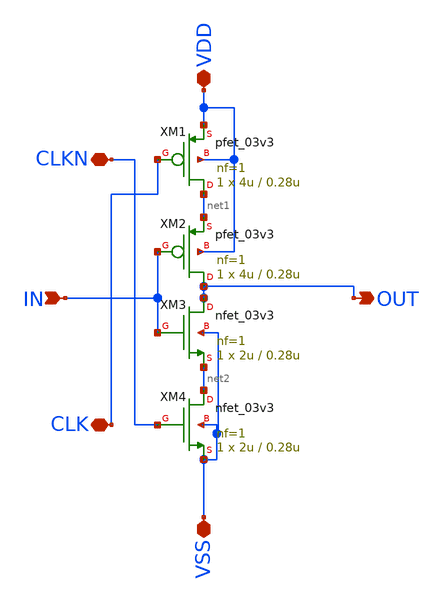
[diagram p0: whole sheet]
** sch_path: CAD6/DFF_Ray/TRI_STATE_INV.sch
**.subckt TRI_STATE_INV VSS VDD CLK CLKN IN OUT
*.iopin VSS
*.iopin VDD
*.iopin CLK
*.iopin CLKN
*.ipin IN
*.opin OUT
XM1 net1 CLK VDD VDD pfet_03v3 L=0.28u W=4u nf=1 ad='int((nf+1)/2) * W/nf * 0.18u' as='int((nf+2)/2) * W/nf * 0.18u'
+ pd='2*int((nf+1)/2) * (W/nf + 0.18u)' ps='2*int((nf+2)/2) * (W/nf + 0.18u)' nrd='0.18u / W' nrs='0.18u / W'
+ sa=0 sb=0 sd=0 m=1
XM2 OUT IN net1 VDD pfet_03v3 L=0.28u W=4u nf=1 ad='int((nf+1)/2) * W/nf * 0.18u' as='int((nf+2)/2) * W/nf * 0.18u'
+ pd='2*int((nf+1)/2) * (W/nf + 0.18u)' ps='2*int((nf+2)/2) * (W/nf + 0.18u)' nrd='0.18u / W' nrs='0.18u / W'
+ sa=0 sb=0 sd=0 m=1
XM3 OUT IN net2 VSS nfet_03v3 L=0.28u W=2u nf=1 ad='int((nf+1)/2) * W/nf * 0.18u' as='int((nf+2)/2) * W/nf * 0.18u'
+ pd='2*int((nf+1)/2) * (W/nf + 0.18u)' ps='2*int((nf+2)/2) * (W/nf + 0.18u)' nrd='0.18u / W' nrs='0.18u / W'
+ sa=0 sb=0 sd=0 m=1
XM4 net2 CLKN VSS VSS nfet_03v3 L=0.28u W=2u nf=1 ad='int((nf+1)/2) * W/nf * 0.18u' as='int((nf+2)/2) * W/nf * 0.18u'
+ pd='2*int((nf+1)/2) * (W/nf + 0.18u)' ps='2*int((nf+2)/2) * (W/nf + 0.18u)' nrd='0.18u / W' nrs='0.18u / W'
+ sa=0 sb=0 sd=0 m=1
**.ends
.end
